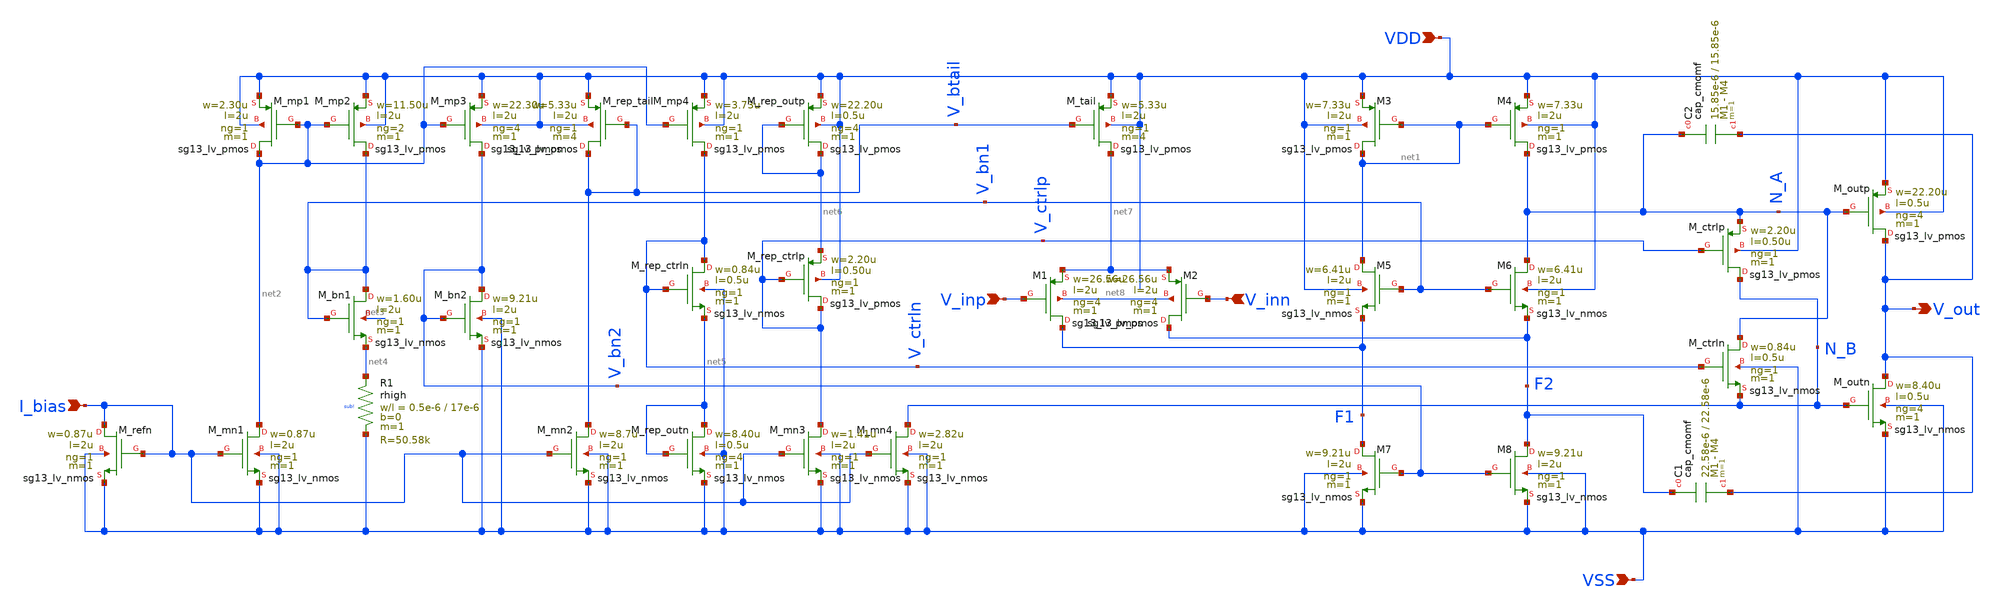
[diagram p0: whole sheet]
** sch_path: designs/libs/core_analog/coarse_gain/cg_ota.sch
**.subckt cg_ota V_inp VDD VSS V_out I_bias V_inn
*.ipin V_inp
*.ipin VDD
*.ipin VSS
*.opin V_out
*.ipin I_bias
*.ipin V_inn
XM1 F1 V_inp net7 net8 sg13_lv_pmos w=26.56u l=2u ng=4 m=1 mm_ok=1
XM2 F2 V_inn net7 net8 sg13_lv_pmos w=26.56u l=2u ng=4 m=1 mm_ok=1
XM3 net1 net1 VDD VDD sg13_lv_pmos w=7.33u l=2u ng=1 m=1 mm_ok=1
XM4 N_A net1 VDD VDD sg13_lv_pmos w=7.33u l=2u ng=1 m=1 mm_ok=1
XM7 F1 V_bn2 VSS VSS sg13_lv_nmos w=9.21u l=2u ng=1 m=1 mm_ok=1
XM8 F2 V_bn2 VSS VSS sg13_lv_nmos w=9.21u l=2u ng=1 m=1 mm_ok=1
XM_tail net7 V_btail VDD VDD sg13_lv_pmos w=5.33u l=2u ng=1 m=4 mm_ok=1
XM_ctrlp N_B V_ctrlp N_A VDD sg13_lv_pmos w=2.20u l=0.50u ng=1 m=1 mm_ok=1
XM_outp V_out N_A VDD VDD sg13_lv_pmos w=22.20u l=0.5u ng=4 m=1 mm_ok=1
XM_ctrln N_A V_ctrln N_B VSS sg13_lv_nmos w=0.84u l=0.5u ng=1 m=1 mm_ok=1
XM_outn V_out N_B VSS VSS sg13_lv_nmos w=8.40u l=0.5u ng=4 m=1 mm_ok=1
XM5 net1 V_bn1 F1 VDD sg13_lv_nmos w=6.41u l=2u ng=1 m=1 mm_ok=1
XM6 N_A V_bn1 F2 VDD sg13_lv_nmos w=6.41u l=2u ng=1 m=1 mm_ok=1
XM_mp1 net2 net2 VDD VDD sg13_lv_pmos w=2.30u l=2u ng=1 m=1 mm_ok=1
XM_mn1 net2 I_bias VSS VSS sg13_lv_nmos w=0.87u l=2u ng=1 m=1 mm_ok=1
XM_refn I_bias I_bias VSS VSS sg13_lv_nmos w=0.87u l=2u ng=1 m=1 mm_ok=1
XM_mp2 V_bn1 net2 VDD VDD sg13_lv_pmos w=11.50u l=2u ng=2 m=1 mm_ok=1
XM_mp3 V_bn2 net2 VDD VDD sg13_lv_pmos w=22.30u l=2u ng=4 m=1 mm_ok=1
XM_bn1 V_bn1 V_bn1 net4 net3 sg13_lv_nmos w=1.60u l=2u ng=1 m=1 mm_ok=1
XM_bn2 V_bn2 V_bn2 VSS VSS sg13_lv_nmos w=9.21u l=2u ng=1 m=1 mm_ok=1
XM_mn2 V_btail I_bias VSS VSS sg13_lv_nmos w=8.7u l=2u ng=1 m=1 mm_ok=1
XM_rep_tail V_btail V_btail VDD VDD sg13_lv_pmos w=5.33u l=2u ng=1 m=4 mm_ok=1
XM_mn4 N_B I_bias VSS VSS sg13_lv_nmos w=2.82u l=2u ng=1 m=1 mm_ok=1
XC1 F2 V_out cap_cmomf w=22.58e-6 l=22.58e-6 mmin=1 mmax=4 subblock=0 rfmodel=0 subscale=1 m=1
+ mm_ok=1
XC2 N_A V_out cap_cmomf w=15.85e-6 l=15.85e-6 mmin=1 mmax=4 subblock=0 rfmodel=0 subscale=1 m=1
+ mm_ok=1
XR1 net4 VSS sub! rhigh w=0.5e-6 l=17e-6 m=1 b=0 mm_ok=1
XM_mp4 V_ctrln net2 VDD VDD sg13_lv_pmos w=3.73u l=2u ng=1 m=1 mm_ok=1
XM_rep_ctrln V_ctrln V_ctrln net5 VSS sg13_lv_nmos w=0.84u l=0.5u ng=1 m=1 mm_ok=1
XM_rep_outn net5 net5 VSS VSS sg13_lv_nmos w=8.40u l=0.5u ng=4 m=1 mm_ok=1
XM_mn3 V_ctrlp I_bias VSS VSS sg13_lv_nmos w=1.41u l=2u ng=1 m=1 mm_ok=1
XM_rep_outp net6 net6 VDD VDD sg13_lv_pmos w=22.20u l=0.5u ng=4 m=1 mm_ok=1
XM_rep_ctrlp V_ctrlp V_ctrlp net6 VDD sg13_lv_pmos w=2.20u l=0.50u ng=1 m=1 mm_ok=1
**.ends
.end
